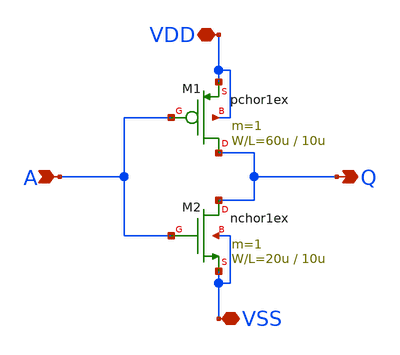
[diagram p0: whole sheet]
** sch_path: member_project/hiro-ogawa/inverter.sch
**.subckt inverter A Q VDD VSS
*.ipin A
*.opin Q
*.iopin VDD
*.iopin VSS
M1 Q A VDD VDD pchor1ex L=10u W=60u m=1
M2 Q A VSS VSS nchor1ex L=10u W=20u m=1
**.ends
.end
